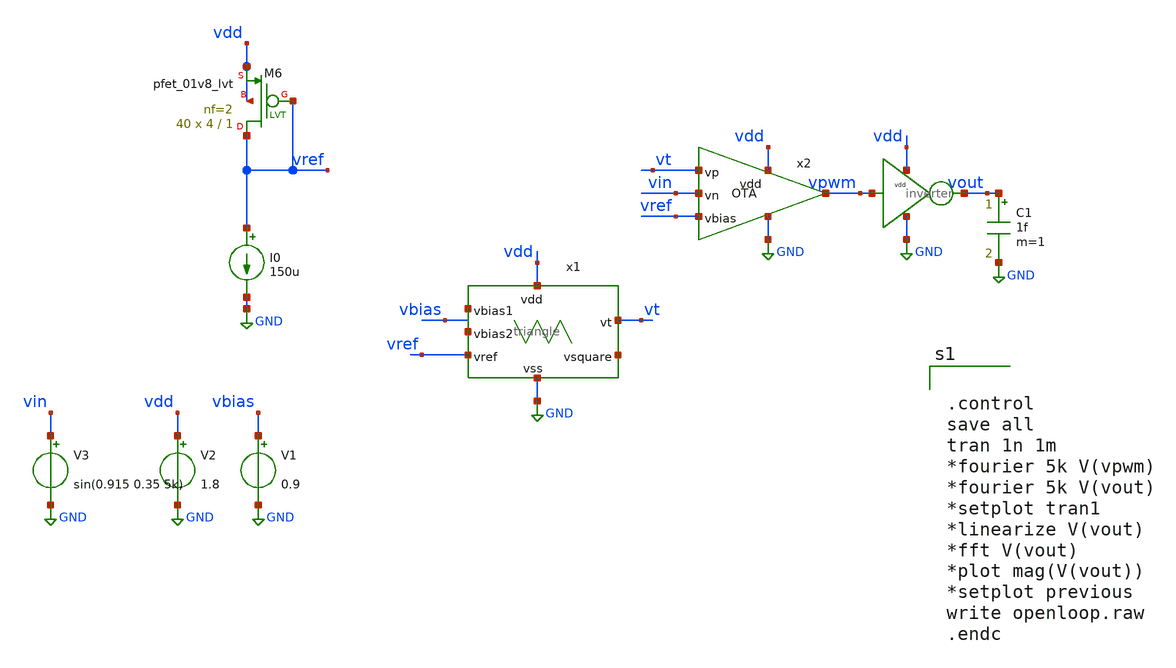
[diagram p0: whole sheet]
** sch_path: xschem/src/openloop/openloop.sch
**.subckt openloop
x1 vdd net1 net2 vref GND net3 vt triangle
x2 vdd vt vin vref GND vpwm OTA
V1 vbias GND 0.9
V2 vdd GND 1.8
XM6 vref vref vdd vdd sky130_fd_pr__pfet_01v8_lvt L=1 W=4 nf=2 ad='int((nf+1)/2) * W/nf * 0.29' as='int((nf+2)/2) * W/nf * 0.29'
+ pd='2*int((nf+1)/2) * (W/nf + 0.29)' ps='2*int((nf+2)/2) * (W/nf + 0.29)' nrd='0.29 / W' nrs='0.29 / W'
+ sa=0 sb=0 sd=0 mult=40 m=40
I0 vref GND 150u
V3 vin GND sin(0.915 0.35 5k)
x3 vdd vpwm vout GND inverter
C1 vout GND 1f m=1
**** begin user architecture code

.include /home/eda/pdk/skywater-pdk/libraries/sky130_fd_pr_ngspice/latest/models/corners/tt.spice


* Resistor$::SKYWATER_MODELS/Capacitor
.include $::SKYWATER_MODELS/models/r+c/res_typical__cap_typical.spice
.include $::SKYWATER_MODELS/models/r+c/res_typical__cap_typical__lin.spice
* Special cells
.include $::SKYWATER_MODELS/models/corners/tt/specialized_cells.spice




.control
save all
tran 1n 1m
*fourier 5k V(vpwm)
*fourier 5k V(vout)
*setplot tran1
*linearize V(vout)
*fft V(vout)
*plot mag(V(vout))
*setplot previous
write openloop.raw
.endc


**** end user architecture code
**.ends

* expanding   symbol:  src/triangle/triangle.sym # of pins=7
** sym_path: xschem/src/triangle/triangle.sym
** sch_path: xschem/src/triangle/triangle.sch
.subckt triangle vdd vbias1 vbias2 vref vss vsquare vt
*.iopin vdd
*.ipin vbias1
*.opin vt
*.ipin vref
*.opin vsquare
*.iopin vss
*.ipin vbias2
XR3 vsquare vi vss sky130_fd_pr__res_xhigh_po L=32 mult=1 m=1
XR1 vt vcmp vss sky130_fd_pr__res_xhigh_po L=4 mult=1 m=1
XR2 vcmp vsquare vss sky130_fd_pr__res_xhigh_po L=9 mult=1 m=1
x1 vdd vref vi vbias1 vss vt OTA_tri
x2 vdd vcmp vref vbias2 vss vsquare OTA
XC1 vi vt sky130_fd_pr__cap_mim_m3_1 W=15 L=15 MF=8 m=8
.ends


* expanding   symbol:  src/OTA/OTA.sym # of pins=6
** sym_path: xschem/src/OTA/OTA.sym
** sch_path: xschem/src/OTA/OTA.sch
.subckt OTA vdd vp vn vbias vss vout
*.ipin vp
*.ipin vn
*.ipin vbias
*.iopin vss
*.iopin vdd
*.opin vout
XM1 v1 vp vc vc sky130_fd_pr__pfet_01v8_lvt L=1 W=4 nf=1 ad='int((nf+1)/2) * W/nf * 0.29' as='int((nf+2)/2) * W/nf * 0.29'
+ pd='2*int((nf+1)/2) * (W/nf + 0.29)' ps='2*int((nf+2)/2) * (W/nf + 0.29)' nrd='0.29 / W' nrs='0.29 / W'
+ sa=0 sb=0 sd=0 mult=16 m=16
XM2 vf vn vc vc sky130_fd_pr__pfet_01v8_lvt L=1 W=4 nf=1 ad='int((nf+1)/2) * W/nf * 0.29' as='int((nf+2)/2) * W/nf * 0.29'
+ pd='2*int((nf+1)/2) * (W/nf + 0.29)' ps='2*int((nf+2)/2) * (W/nf + 0.29)' nrd='0.29 / W' nrs='0.29 / W'
+ sa=0 sb=0 sd=0 mult=16 m=16
XM3 vc vbias vdd vdd sky130_fd_pr__pfet_01v8_lvt L=1 W=2 nf=2 ad='int((nf+1)/2) * W/nf * 0.29' as='int((nf+2)/2) * W/nf * 0.29'
+ pd='2*int((nf+1)/2) * (W/nf + 0.29)' ps='2*int((nf+2)/2) * (W/nf + 0.29)' nrd='0.29 / W' nrs='0.29 / W'
+ sa=0 sb=0 sd=0 mult=24 m=24
XM4 v1 vf vss vss sky130_fd_pr__nfet_01v8_lvt L=1 W=1 nf=1 ad='int((nf+1)/2) * W/nf * 0.29' as='int((nf+2)/2) * W/nf * 0.29'
+ pd='2*int((nf+1)/2) * (W/nf + 0.29)' ps='2*int((nf+2)/2) * (W/nf + 0.29)' nrd='0.29 / W' nrs='0.29 / W'
+ sa=0 sb=0 sd=0 mult=16 m=16
XM5 vf vf vss vss sky130_fd_pr__nfet_01v8_lvt L=1 W=1 nf=1 ad='int((nf+1)/2) * W/nf * 0.29' as='int((nf+2)/2) * W/nf * 0.29'
+ pd='2*int((nf+1)/2) * (W/nf + 0.29)' ps='2*int((nf+2)/2) * (W/nf + 0.29)' nrd='0.29 / W' nrs='0.29 / W'
+ sa=0 sb=0 sd=0 mult=16 m=16
XM6 vbias vbias vdd vdd sky130_fd_pr__pfet_01v8_lvt L=1 W=2 nf=2 ad='int((nf+1)/2) * W/nf * 0.29' as='int((nf+2)/2) * W/nf * 0.29'
+ pd='2*int((nf+1)/2) * (W/nf + 0.29)' ps='2*int((nf+2)/2) * (W/nf + 0.29)' nrd='0.29 / W' nrs='0.29 / W'
+ sa=0 sb=0 sd=0 mult=24 m=24
XM7 vout vbias vdd vdd sky130_fd_pr__pfet_01v8_lvt L=1 W=2 nf=2 ad='int((nf+1)/2) * W/nf * 0.29' as='int((nf+2)/2) * W/nf * 0.29'
+ pd='2*int((nf+1)/2) * (W/nf + 0.29)' ps='2*int((nf+2)/2) * (W/nf + 0.29)' nrd='0.29 / W' nrs='0.29 / W'
+ sa=0 sb=0 sd=0 mult=48 m=48
XM8 vout v1 vss vss sky130_fd_pr__nfet_01v8_lvt L=1 W=1 nf=1 ad='int((nf+1)/2) * W/nf * 0.29' as='int((nf+2)/2) * W/nf * 0.29'
+ pd='2*int((nf+1)/2) * (W/nf + 0.29)' ps='2*int((nf+2)/2) * (W/nf + 0.29)' nrd='0.29 / W' nrs='0.29 / W'
+ sa=0 sb=0 sd=0 mult=64 m=64
XR1 v1 net1 vss sky130_fd_pr__res_xhigh_po W=0.35 L=0.5 mult=1 m=1
XC2 net1 vout sky130_fd_pr__cap_mim_m3_1 W=14 L=14 MF=1 m=1
.ends


* expanding   symbol:  src/inverter/inverter.sym # of pins=4
** sym_path: xschem/src/inverter/inverter.sym
** sch_path: xschem/src/inverter/inverter.sch
.subckt inverter vdd A B vss
*.iopin vdd
*.iopin vss
*.ipin A
*.opin B
XM3 B A vss vss sky130_fd_pr__nfet_01v8 L=0.15 W=1 nf=1 ad='int((nf+1)/2) * W/nf * 0.29' as='int((nf+2)/2) * W/nf * 0.29'
+ pd='2*int((nf+1)/2) * (W/nf + 0.29)' ps='2*int((nf+2)/2) * (W/nf + 0.29)' nrd='0.29 / W' nrs='0.29 / W'
+ sa=0 sb=0 sd=0 mult=1 m=1
XM1 B A vdd vdd sky130_fd_pr__pfet_01v8 L=0.15 W=2 nf=1 ad='int((nf+1)/2) * W/nf * 0.29' as='int((nf+2)/2) * W/nf * 0.29'
+ pd='2*int((nf+1)/2) * (W/nf + 0.29)' ps='2*int((nf+2)/2) * (W/nf + 0.29)' nrd='0.29 / W' nrs='0.29 / W'
+ sa=0 sb=0 sd=0 mult=1 m=1
.ends


* expanding   symbol:  src/OTA_tri/OTA_tri.sym # of pins=6
** sym_path: xschem/src/OTA_tri/OTA_tri.sym
** sch_path: xschem/src/OTA_tri/OTA_tri.sch
.subckt OTA_tri vdd vp vn vbias vss vout
*.ipin vp
*.ipin vn
*.ipin vbias
*.iopin vss
*.iopin vdd
*.opin vout
XM1 v1 vp vc vc sky130_fd_pr__pfet_01v8_lvt L=1 W=4 nf=1 ad='int((nf+1)/2) * W/nf * 0.29' as='int((nf+2)/2) * W/nf * 0.29'
+ pd='2*int((nf+1)/2) * (W/nf + 0.29)' ps='2*int((nf+2)/2) * (W/nf + 0.29)' nrd='0.29 / W' nrs='0.29 / W'
+ sa=0 sb=0 sd=0 mult=16 m=16
XM2 vf vn vc vc sky130_fd_pr__pfet_01v8_lvt L=1 W=4 nf=1 ad='int((nf+1)/2) * W/nf * 0.29' as='int((nf+2)/2) * W/nf * 0.29'
+ pd='2*int((nf+1)/2) * (W/nf + 0.29)' ps='2*int((nf+2)/2) * (W/nf + 0.29)' nrd='0.29 / W' nrs='0.29 / W'
+ sa=0 sb=0 sd=0 mult=16 m=16
XM3 vc vbias vdd vdd sky130_fd_pr__pfet_01v8_lvt L=1 W=2 nf=2 ad='int((nf+1)/2) * W/nf * 0.29' as='int((nf+2)/2) * W/nf * 0.29'
+ pd='2*int((nf+1)/2) * (W/nf + 0.29)' ps='2*int((nf+2)/2) * (W/nf + 0.29)' nrd='0.29 / W' nrs='0.29 / W'
+ sa=0 sb=0 sd=0 mult=24 m=24
XM4 v1 vf vss vss sky130_fd_pr__nfet_01v8_lvt L=1 W=1 nf=1 ad='int((nf+1)/2) * W/nf * 0.29' as='int((nf+2)/2) * W/nf * 0.29'
+ pd='2*int((nf+1)/2) * (W/nf + 0.29)' ps='2*int((nf+2)/2) * (W/nf + 0.29)' nrd='0.29 / W' nrs='0.29 / W'
+ sa=0 sb=0 sd=0 mult=16 m=16
XM5 vf vf vss vss sky130_fd_pr__nfet_01v8_lvt L=1 W=1 nf=1 ad='int((nf+1)/2) * W/nf * 0.29' as='int((nf+2)/2) * W/nf * 0.29'
+ pd='2*int((nf+1)/2) * (W/nf + 0.29)' ps='2*int((nf+2)/2) * (W/nf + 0.29)' nrd='0.29 / W' nrs='0.29 / W'
+ sa=0 sb=0 sd=0 mult=16 m=16
XM6 vbias vbias vdd vdd sky130_fd_pr__pfet_01v8_lvt L=1 W=2 nf=2 ad='int((nf+1)/2) * W/nf * 0.29' as='int((nf+2)/2) * W/nf * 0.29'
+ pd='2*int((nf+1)/2) * (W/nf + 0.29)' ps='2*int((nf+2)/2) * (W/nf + 0.29)' nrd='0.29 / W' nrs='0.29 / W'
+ sa=0 sb=0 sd=0 mult=24 m=24
XM7 vout vbias vdd vdd sky130_fd_pr__pfet_01v8_lvt L=1 W=2 nf=3 ad='int((nf+1)/2) * W/nf * 0.29' as='int((nf+2)/2) * W/nf * 0.29'
+ pd='2*int((nf+1)/2) * (W/nf + 0.29)' ps='2*int((nf+2)/2) * (W/nf + 0.29)' nrd='0.29 / W' nrs='0.29 / W'
+ sa=0 sb=0 sd=0 mult=48 m=48
XM8 vout v1 vss vss sky130_fd_pr__nfet_01v8_lvt L=1 W=1 nf=1 ad='int((nf+1)/2) * W/nf * 0.29' as='int((nf+2)/2) * W/nf * 0.29'
+ pd='2*int((nf+1)/2) * (W/nf + 0.29)' ps='2*int((nf+2)/2) * (W/nf + 0.29)' nrd='0.29 / W' nrs='0.29 / W'
+ sa=0 sb=0 sd=0 mult=64 m=64
XC1 net1 vout sky130_fd_pr__cap_mim_m3_1 W=27 L=18 MF=1 m=1
XR1 v1 net1 vss sky130_fd_pr__res_xhigh_po W=0.35 L=1.4 mult=1 m=1
.ends

.GLOBAL GND
.end
